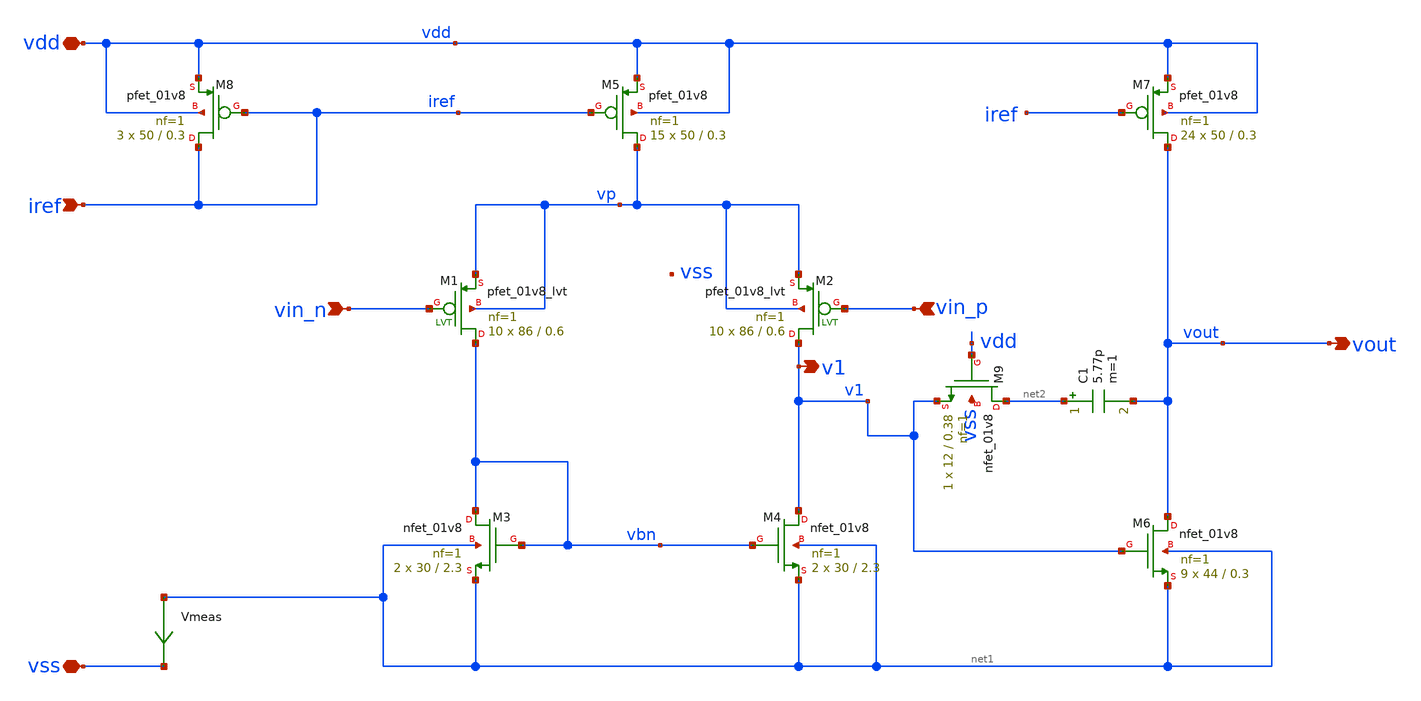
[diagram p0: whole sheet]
** sch_path: opamp/opamp.sch
**.subckt opamp vdd vss vin_n vin_p iref vout v1
*.iopin vdd
*.iopin vss
*.ipin vin_n
*.ipin vin_p
*.ipin iref
*.opin vout
*.opin v1
XM5 vp iref vdd vdd sky130_fd_pr__pfet_01v8 L=0.3 W=50 nf=1 ad='W * 0.29' as='W * 0.29' pd='2 * (W + 0.29)'
+ ps='2 * (W + 0.29)' nrd='0.29 / W' nrs='0.29 / W' sa=0 sb=0 sd=0 mult=15 m=15
XM7 vout iref vdd vdd sky130_fd_pr__pfet_01v8 L=0.3 W=50 nf=1 ad='W * 0.29' as='W * 0.29' pd='2 * (W + 0.29)'
+ ps='2 * (W + 0.29)' nrd='0.29 / W' nrs='0.29 / W' sa=0 sb=0 sd=0 mult=24 m=24
XM8 iref iref vdd vdd sky130_fd_pr__pfet_01v8 L=0.3 W=50 nf=1 ad='W * 0.29' as='W * 0.29' pd='2 * (W + 0.29)'
+ ps='2 * (W + 0.29)' nrd='0.29 / W' nrs='0.29 / W' sa=0 sb=0 sd=0 mult=3 m=3
XM1 vbn vin_n vp vp sky130_fd_pr__pfet_01v8_lvt L=0.6 W=86 nf=1 ad='int((nf+1)/2) * W/nf * 0.29' as='int((nf+2)/2) * W/nf * 0.29'
+ pd='2*int((nf+1)/2) * (W/nf + 0.29)' ps='2*int((nf+2)/2) * (W/nf + 0.29)' nrd='0.29 / W' nrs='0.29 / W'
+ sa=0 sb=0 sd=0 mult=10 m=10
XM2 v1 vin_p vp vp sky130_fd_pr__pfet_01v8_lvt L=0.6 W=86 nf=1 ad='int((nf+1)/2) * W/nf * 0.29' as='int((nf+2)/2) * W/nf * 0.29'
+ pd='2*int((nf+1)/2) * (W/nf + 0.29)' ps='2*int((nf+2)/2) * (W/nf + 0.29)' nrd='0.29 / W' nrs='0.29 / W'
+ sa=0 sb=0 sd=0 mult=10 m=10
C1 net2 vout 5.77p m=1
Vmeas net1 vss 0
.save i(vmeas)
XM6 vout v1 net1 net1 sky130_fd_pr__nfet_01v8 L=0.3 W=44 nf=1 ad='W * 0.29' as='W * 0.29' pd='2 * (W + 0.29)'
+ ps='2 * (W + 0.29)' nrd='0.29 / W' nrs='0.29 / W' sa=0 sb=0 sd=0 mult=9 m=9
XM4 v1 vbn net1 net1 sky130_fd_pr__nfet_01v8 L=2.3 W=30 nf=1 ad='W * 0.29' as='W * 0.29' pd='2 * (W + 0.29)'
+ ps='2 * (W + 0.29)' nrd='0.29 / W' nrs='0.29 / W' sa=0 sb=0 sd=0 mult=2 m=2
XM3 vbn vbn net1 net1 sky130_fd_pr__nfet_01v8 L=2.3 W=30 nf=1 ad='W * 0.29' as='W * 0.29' pd='2 * (W + 0.29)'
+ ps='2 * (W + 0.29)' nrd='0.29 / W' nrs='0.29 / W' sa=0 sb=0 sd=0 mult=2 m=2
XM9 net2 vdd v1 vss sky130_fd_pr__nfet_01v8 L=0.38 W=12 nf=1 ad='W * 0.29' as='W * 0.29' pd='2 * (W + 0.29)'
+ ps='2 * (W + 0.29)' nrd='0.29 / W' nrs='0.29 / W' sa=0 sb=0 sd=0 mult=1 m=1
**.ends
.end
